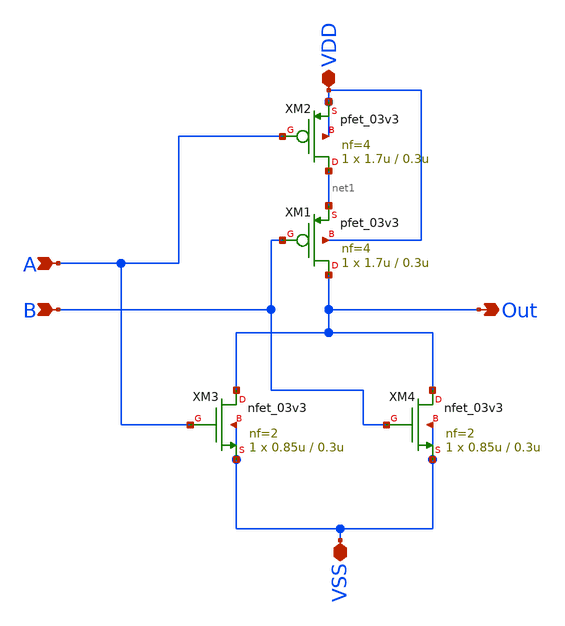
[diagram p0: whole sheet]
** sch_path: cells/comp4/comp4_2x/schematic/my_nor_2x.sch
**.subckt my_nor_2x A B VDD VSS Out
*.ipin A
*.ipin B
*.iopin VDD
*.iopin VSS
*.opin Out
XM2 net1 A VDD VDD pfet_03v3 L=0.3u W=1.7u nf=4 ad='int((nf+1)/2) * W/nf * 0.18u' as='int((nf+2)/2) * W/nf * 0.18u'
+ pd='2*int((nf+1)/2) * (W/nf + 0.18u)' ps='2*int((nf+2)/2) * (W/nf + 0.18u)' nrd='0.18u / W' nrs='0.18u / W'
+ sa=0 sb=0 sd=0 m=1
XM1 Out B net1 VDD pfet_03v3 L=0.3u W=1.7u nf=4 ad='int((nf+1)/2) * W/nf * 0.18u' as='int((nf+2)/2) * W/nf * 0.18u'
+ pd='2*int((nf+1)/2) * (W/nf + 0.18u)' ps='2*int((nf+2)/2) * (W/nf + 0.18u)' nrd='0.18u / W' nrs='0.18u / W'
+ sa=0 sb=0 sd=0 m=1
XM3 Out A VSS VSS nfet_03v3 L=0.3u W=0.85u nf=2 ad='int((nf+1)/2) * W/nf * 0.18u' as='int((nf+2)/2) * W/nf * 0.18u'
+ pd='2*int((nf+1)/2) * (W/nf + 0.18u)' ps='2*int((nf+2)/2) * (W/nf + 0.18u)' nrd='0.18u / W' nrs='0.18u / W'
+ sa=0 sb=0 sd=0 m=1
XM4 Out B VSS VSS nfet_03v3 L=0.3u W=0.85u nf=2 ad='int((nf+1)/2) * W/nf * 0.18u' as='int((nf+2)/2) * W/nf * 0.18u'
+ pd='2*int((nf+1)/2) * (W/nf + 0.18u)' ps='2*int((nf+2)/2) * (W/nf + 0.18u)' nrd='0.18u / W' nrs='0.18u / W'
+ sa=0 sb=0 sd=0 m=1
**.ends
.end
